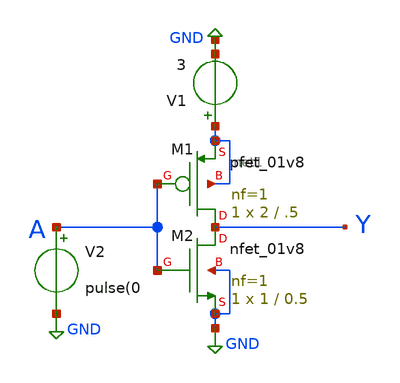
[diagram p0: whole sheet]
** sch_path: xschem_sky130/EE_431_Inverter.sch
**.subckt EE_431_Inverter
XM2 Y A GND GND sky130_fd_pr__nfet_01v8 L=0.5 W=1 nf=1 ad='int((1 + 1)/2) * 1 / 1 * 0.29' as='int((1 + 2)/2) * 1 / 1 * 0.29'
+ pd='2*int((1 + 1)/2) * (1 / 1 + 0.29)' ps='2*int((1 + 2)/2) * (1 / 1 + 0.29)' nrd='0.29 / 1 ' nrs='0.29 / 1 '
+ sa=0 sb=0 sd=0 mult=1 m=1
XM1 Y A net1 net1 sky130_fd_pr__pfet_01v8 L=.5 W=2 nf=1 ad='int((1 + 1)/2) * 2 / 1 * 0.29' as='int((1 + 2)/2) * 2 / 1 * 0.29'
+ pd='2*int((1 + 1)/2) * (2 / 1 + 0.29)' ps='2*int((1 + 2)/2) * (2 / 1 + 0.29)' nrd='0.29 / 2 ' nrs='0.29 / 2 '
+ sa=0 sb=0 sd=0 mult=1 m=1
V1 net1 net2 3
V2 A GND pulse(0
**.ends
.GLOBAL GND
.end
